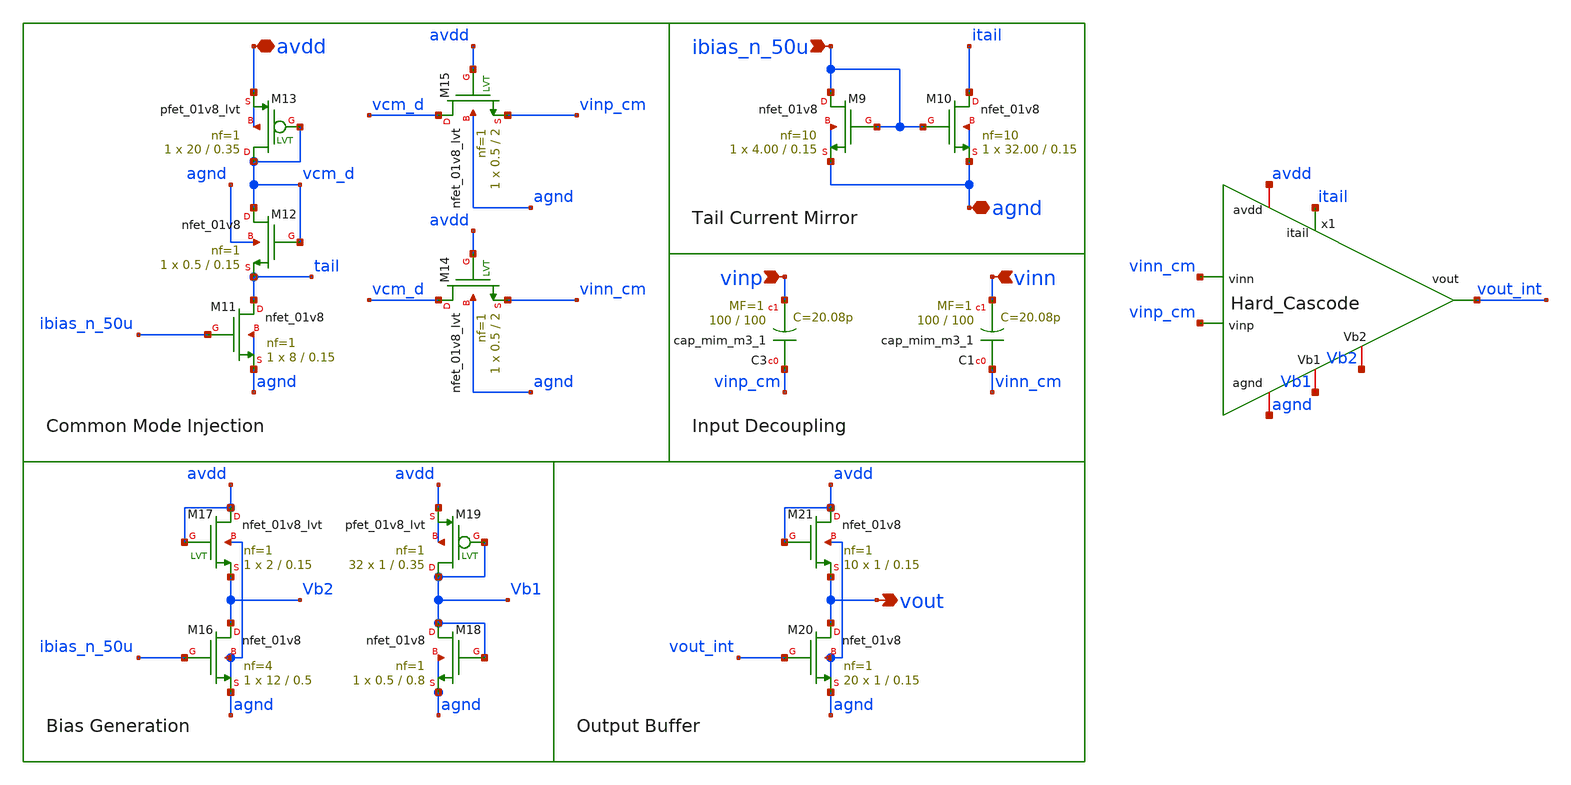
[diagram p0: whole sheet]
** sch_path: AMP/Hard_Modules_Amp.sch
**.subckt Hard_Modules_Amp avdd vinp vout agnd vinn ibias_n_50u
*.iopin avdd
*.ipin vinp
*.opin vout
*.iopin agnd
*.ipin vinn
*.ipin ibias_n_50u
XM9 ibias_n_50u ibias_n_50u agnd agnd sky130_fd_pr__nfet_01v8 L=0.15 W=4.00 nf=10 ad='int((nf+1)/2) * W/nf * 0.29'
+ as='int((nf+2)/2) * W/nf * 0.29' pd='2*int((nf+1)/2) * (W/nf + 0.29)' ps='2*int((nf+2)/2) * (W/nf + 0.29)'
+ nrd='0.29 / W' nrs='0.29 / W' sa=0 sb=0 sd=0 mult=1 m=1
XM10 itail ibias_n_50u agnd agnd sky130_fd_pr__nfet_01v8 L=0.15 W=32.00 nf=10 ad='int((nf+1)/2) * W/nf * 0.29'
+ as='int((nf+2)/2) * W/nf * 0.29' pd='2*int((nf+1)/2) * (W/nf + 0.29)' ps='2*int((nf+2)/2) * (W/nf + 0.29)'
+ nrd='0.29 / W' nrs='0.29 / W' sa=0 sb=0 sd=0 mult=1 m=1
XM11 tail ibias_n_50u agnd agnd sky130_fd_pr__nfet_01v8 L=0.15 W=8 nf=1 ad='int((nf+1)/2) * W/nf * 0.29'
+ as='int((nf+2)/2) * W/nf * 0.29' pd='2*int((nf+1)/2) * (W/nf + 0.29)' ps='2*int((nf+2)/2) * (W/nf + 0.29)'
+ nrd='0.29 / W' nrs='0.29 / W' sa=0 sb=0 sd=0 mult=1 m=1
XM12 vcm_d vcm_d tail agnd sky130_fd_pr__nfet_01v8 L=0.15 W=0.5 nf=1 ad='int((nf+1)/2) * W/nf * 0.29'
+ as='int((nf+2)/2) * W/nf * 0.29' pd='2*int((nf+1)/2) * (W/nf + 0.29)' ps='2*int((nf+2)/2) * (W/nf + 0.29)'
+ nrd='0.29 / W' nrs='0.29 / W' sa=0 sb=0 sd=0 mult=1 m=1
XM13 vcm_d vcm_d avdd avdd sky130_fd_pr__pfet_01v8_lvt L=0.35 W=20 nf=1 ad='int((nf+1)/2) * W/nf * 0.29'
+ as='int((nf+2)/2) * W/nf * 0.29' pd='2*int((nf+1)/2) * (W/nf + 0.29)' ps='2*int((nf+2)/2) * (W/nf + 0.29)'
+ nrd='0.29 / W' nrs='0.29 / W' sa=0 sb=0 sd=0 mult=1 m=1
XM14 vcm_d avdd vinn_cm agnd sky130_fd_pr__nfet_01v8_lvt L=2 W=0.5 nf=1 ad='int((nf+1)/2) * W/nf * 0.29'
+ as='int((nf+2)/2) * W/nf * 0.29' pd='2*int((nf+1)/2) * (W/nf + 0.29)' ps='2*int((nf+2)/2) * (W/nf + 0.29)'
+ nrd='0.29 / W' nrs='0.29 / W' sa=0 sb=0 sd=0 mult=1 m=1
XM15 vcm_d avdd vinp_cm agnd sky130_fd_pr__nfet_01v8_lvt L=2 W=0.5 nf=1 ad='int((nf+1)/2) * W/nf * 0.29'
+ as='int((nf+2)/2) * W/nf * 0.29' pd='2*int((nf+1)/2) * (W/nf + 0.29)' ps='2*int((nf+2)/2) * (W/nf + 0.29)'
+ nrd='0.29 / W' nrs='0.29 / W' sa=0 sb=0 sd=0 mult=1 m=1
XC3 vinp_cm vinp sky130_fd_pr__cap_mim_m3_1 W=100 L=100 MF=1 m=1
XC1 vinn_cm vinn sky130_fd_pr__cap_mim_m3_1 W=100 L=100 MF=1 m=1
XM16 Vb2 ibias_n_50u agnd agnd sky130_fd_pr__nfet_01v8 L=0.5 W=12 nf=4 ad='int((nf+1)/2) * W/nf * 0.29'
+ as='int((nf+2)/2) * W/nf * 0.29' pd='2*int((nf+1)/2) * (W/nf + 0.29)' ps='2*int((nf+2)/2) * (W/nf + 0.29)'
+ nrd='0.29 / W' nrs='0.29 / W' sa=0 sb=0 sd=0 mult=1 m=1
XM17 avdd avdd Vb2 agnd sky130_fd_pr__nfet_01v8_lvt L=0.15 W=2 nf=1 ad='int((nf+1)/2) * W/nf * 0.29'
+ as='int((nf+2)/2) * W/nf * 0.29' pd='2*int((nf+1)/2) * (W/nf + 0.29)' ps='2*int((nf+2)/2) * (W/nf + 0.29)'
+ nrd='0.29 / W' nrs='0.29 / W' sa=0 sb=0 sd=0 mult=1 m=1
XM19 Vb1 Vb1 avdd avdd sky130_fd_pr__pfet_01v8_lvt L=0.35 W=1 nf=1 ad='int((nf+1)/2) * W/nf * 0.29' as='int((nf+2)/2) * W/nf * 0.29'
+ pd='2*int((nf+1)/2) * (W/nf + 0.29)' ps='2*int((nf+2)/2) * (W/nf + 0.29)' nrd='0.29 / W' nrs='0.29 / W'
+ sa=0 sb=0 sd=0 mult=32 m=32
XM18 Vb1 Vb1 agnd agnd sky130_fd_pr__nfet_01v8 L=0.8 W=0.5 nf=1 ad='int((nf+1)/2) * W/nf * 0.29' as='int((nf+2)/2) * W/nf * 0.29'
+ pd='2*int((nf+1)/2) * (W/nf + 0.29)' ps='2*int((nf+2)/2) * (W/nf + 0.29)' nrd='0.29 / W' nrs='0.29 / W'
+ sa=0 sb=0 sd=0 mult=1 m=1
XM20 vout vout_int agnd agnd sky130_fd_pr__nfet_01v8 L=0.15 W=1 nf=1 ad='int((nf+1)/2) * W/nf * 0.29'
+ as='int((nf+2)/2) * W/nf * 0.29' pd='2*int((nf+1)/2) * (W/nf + 0.29)' ps='2*int((nf+2)/2) * (W/nf + 0.29)'
+ nrd='0.29 / W' nrs='0.29 / W' sa=0 sb=0 sd=0 mult=20 m=20
XM21 avdd avdd vout agnd sky130_fd_pr__nfet_01v8 L=0.15 W=1 nf=1 ad='int((nf+1)/2) * W/nf * 0.29' as='int((nf+2)/2) * W/nf * 0.29'
+ pd='2*int((nf+1)/2) * (W/nf + 0.29)' ps='2*int((nf+2)/2) * (W/nf + 0.29)' nrd='0.29 / W' nrs='0.29 / W'
+ sa=0 sb=0 sd=0 mult=10 m=10
x1 Vb2 Vb1 avdd vout_int vinn_cm vinp_cm itail agnd Hard_Cascode
**.ends
.end
